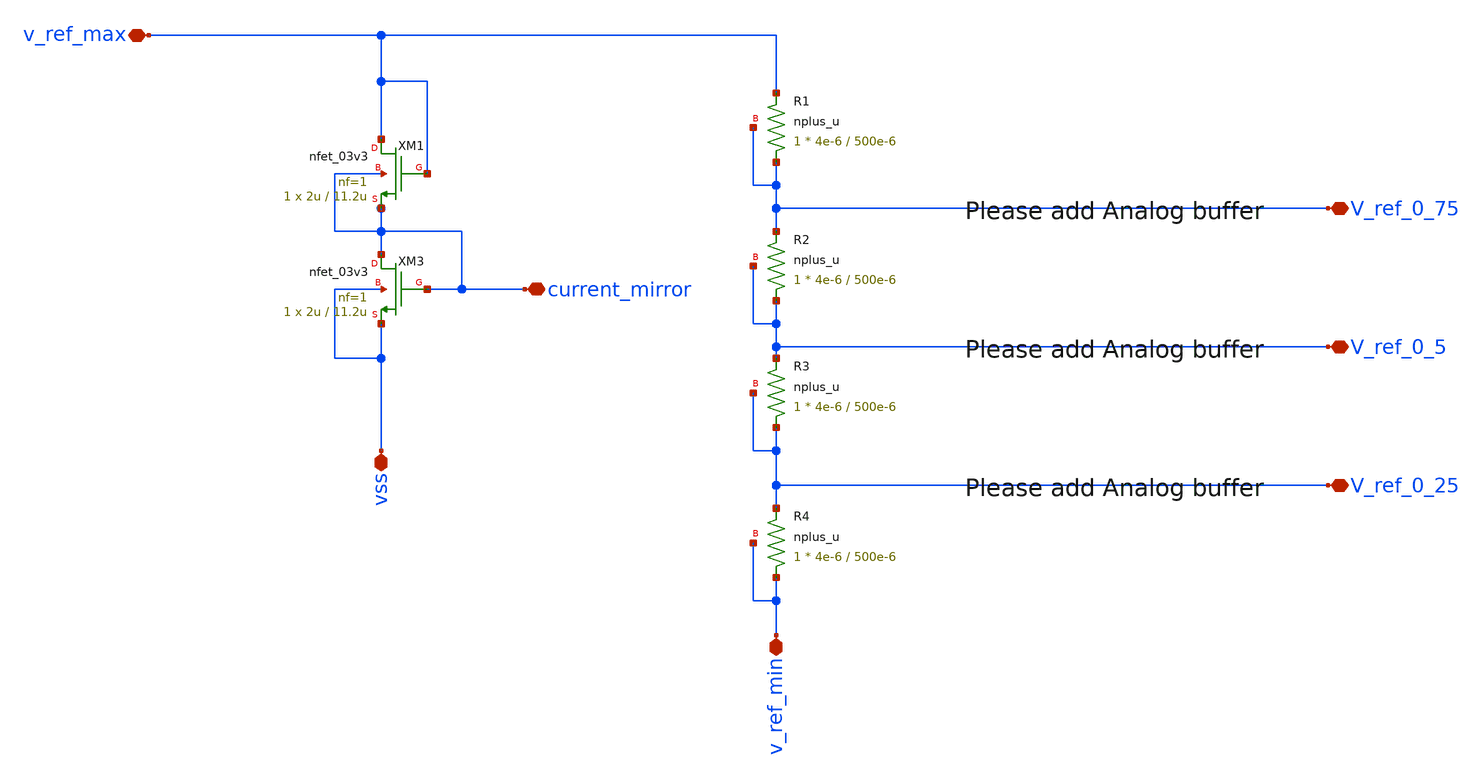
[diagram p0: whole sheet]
** sch_path: General/ADC/Reference/Reference_circuits.sch
**.subckt Reference_circuits v_ref_max vss v_ref_min current_mirror V_ref_0_75 V_ref_0_5 V_ref_0_25
*.iopin v_ref_max
*.iopin vss
*.iopin v_ref_min
*.iopin current_mirror
*.iopin V_ref_0_75
*.iopin V_ref_0_5
*.iopin V_ref_0_25
XR1 V_ref_0_75 v_ref_max V_ref_0_75 nplus_u r_width=4e-6 r_length=500e-6 m=1
XR2 V_ref_0_5 V_ref_0_75 V_ref_0_5 nplus_u r_width=4e-6 r_length=500e-6 m=1
XR3 V_ref_0_25 V_ref_0_5 V_ref_0_25 nplus_u r_width=4e-6 r_length=500e-6 m=1
XR4 v_ref_min V_ref_0_25 v_ref_min nplus_u r_width=4e-6 r_length=500e-6 m=1
XM3 current_mirror current_mirror vss vss nfet_03v3 L=11.2u W=2u nf=1 ad='int((nf+1)/2) * W/nf * 0.18u'
+ as='int((nf+2)/2) * W/nf * 0.18u' pd='2*int((nf+1)/2) * (W/nf + 0.18u)' ps='2*int((nf+2)/2) * (W/nf + 0.18u)'
+ nrd='0.18u / W' nrs='0.18u / W' sa=0 sb=0 sd=0 m=1
XM1 v_ref_max v_ref_max current_mirror current_mirror nfet_03v3 L=11.2u W=2u nf=1 ad='int((nf+1)/2) * W/nf * 0.18u'
+ as='int((nf+2)/2) * W/nf * 0.18u' pd='2*int((nf+1)/2) * (W/nf + 0.18u)' ps='2*int((nf+2)/2) * (W/nf + 0.18u)'
+ nrd='0.18u / W' nrs='0.18u / W' sa=0 sb=0 sd=0 m=1
**.ends
.end
